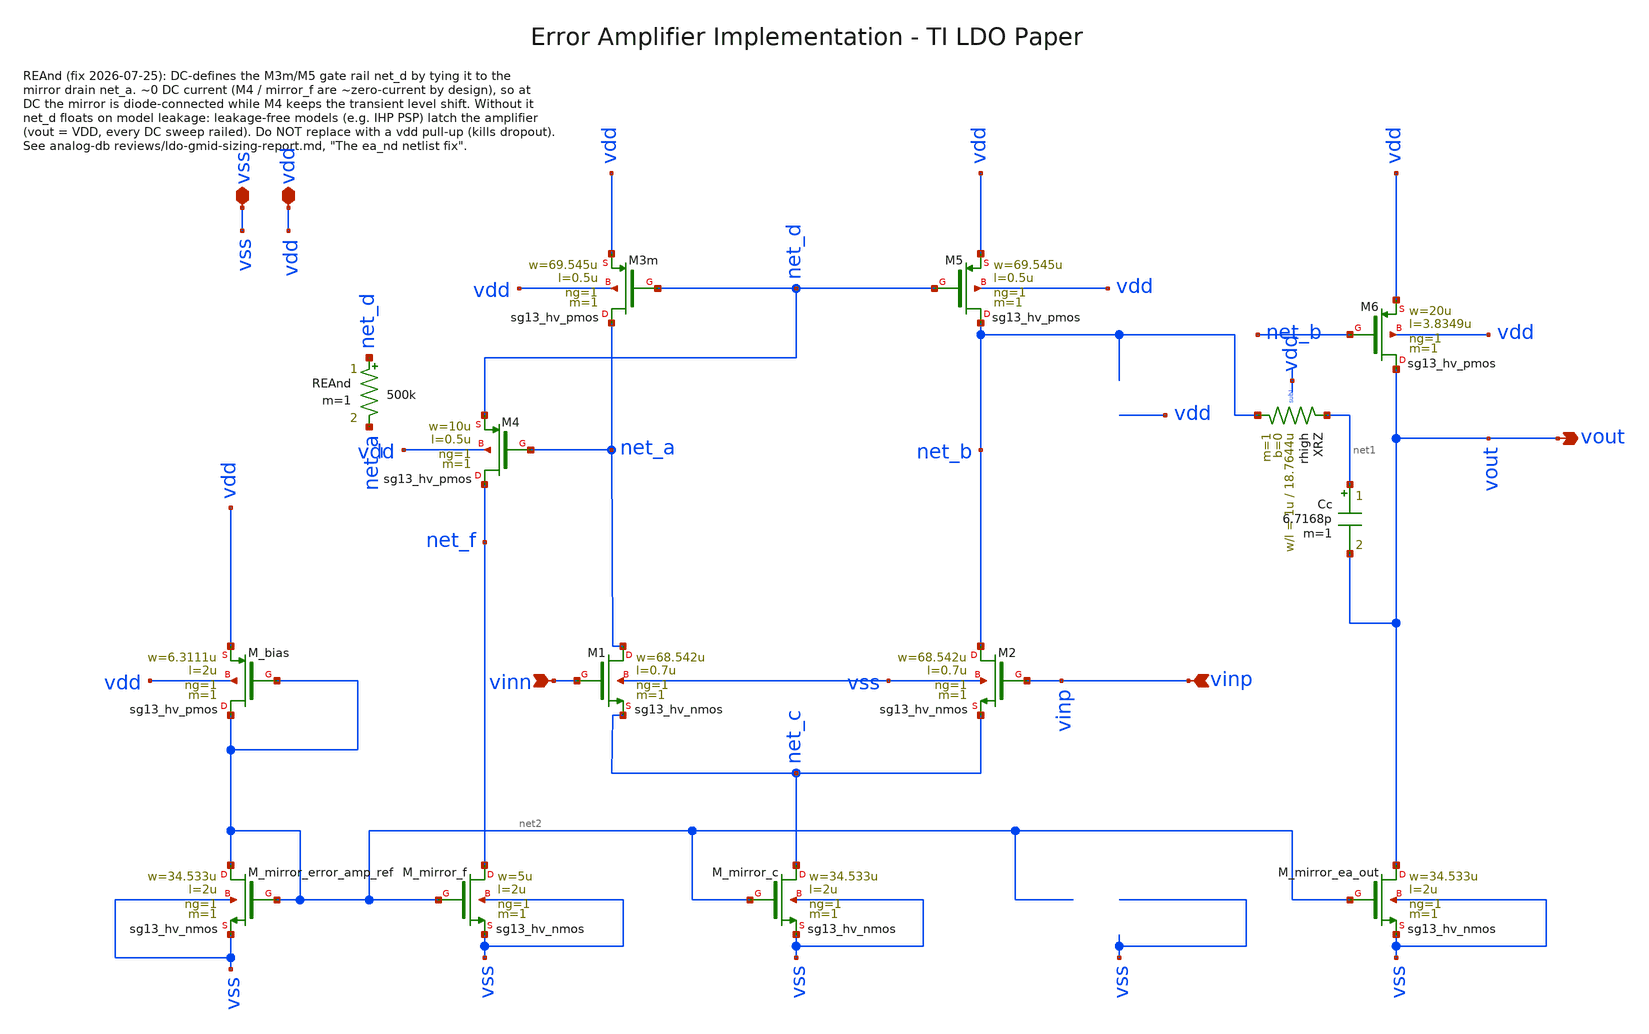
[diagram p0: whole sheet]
** sch_path: analog-db/drawings/ldo-005-ti-ldo-buffer-ref/ihp130/error_amp/error_amp.sch
**.subckt error_amp vdd vss vinp vout vinn
*.iopin vdd
*.iopin vss
*.ipin vinp
*.opin vout
*.ipin vinn
XM2 net_b vinp net_c vss sg13_hv_nmos w=68.542u l=0.7u ng=1 m=1 mm_ok=1
XM3m net_a net_d vdd vdd sg13_hv_pmos w=69.545u l=0.5u ng=1 m=1 mm_ok=1
XM4 net_f net_a net_d vdd sg13_hv_pmos w=10u l=0.5u ng=1 m=1 mm_ok=1
XM5 net_b net_d vdd vdd sg13_hv_pmos w=69.545u l=0.5u ng=1 m=1 mm_ok=1
XM6 vout net_b vdd vdd sg13_hv_pmos w=20u l=3.8349u ng=1 m=1 mm_ok=1
Cc net1 vout 6.7168p m=1
XRZ net_b net1 sub! rhigh w=1u l=18.7644u m=1 b=0
XM1 net_a vinn net_c vss sg13_hv_nmos w=68.542u l=0.7u ng=1 m=1 mm_ok=1
XM_mirror_error_amp_ref net2 net2 vss vss sg13_hv_nmos w=34.533u l=2u ng=1 m=1 mm_ok=1
XM_mirror_f net_f net2 vss vss sg13_hv_nmos w=5u l=2u ng=1 m=1 mm_ok=1
XM_mirror_c net_c net2 vss vss sg13_hv_nmos w=34.533u l=2u ng=1 m=1 mm_ok=1
XM_mirror_ea_out vout net2 vss vss sg13_hv_nmos w=34.533u l=2u ng=1 m=1 mm_ok=1
XM_bias net2 net2 vdd vdd sg13_hv_pmos w=6.3111u l=2u ng=1 m=1 mm_ok=1
REAnd net_d net_a 500k m=1
**.ends
.end
